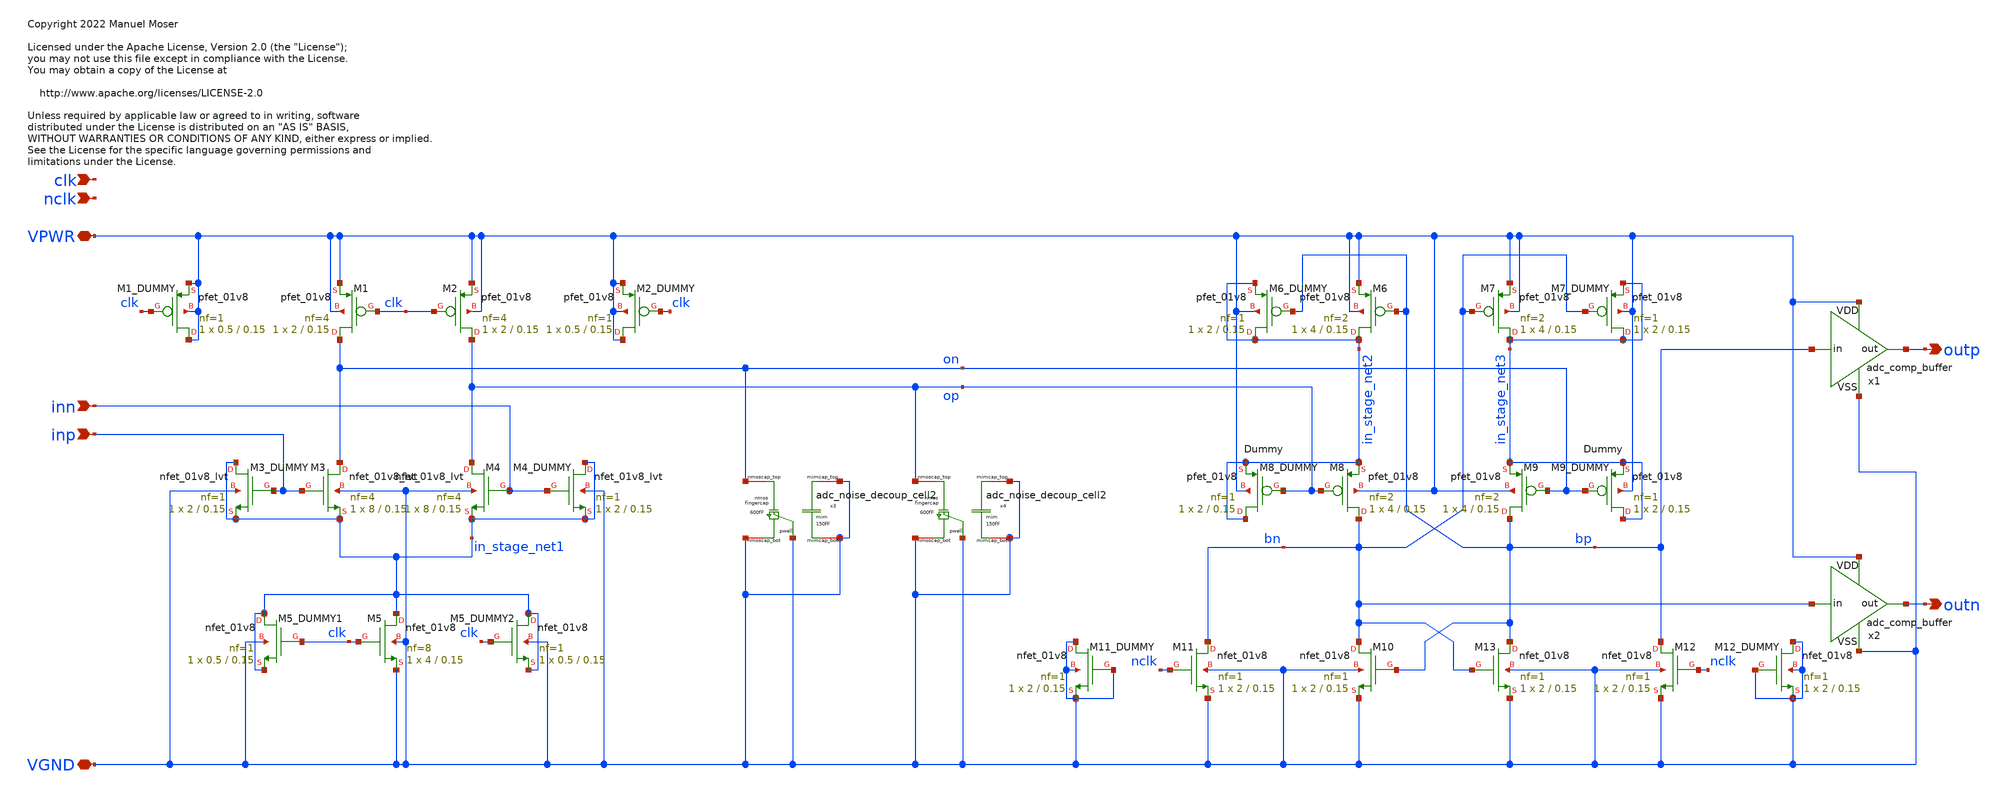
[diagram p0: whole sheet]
** sch_path: xschem/adc_comp_circuit.sch
* Copyright 2022 Manuel Moser
* Licensed under the Apache License, Version 2.0 (the "License");
**.subckt adc_comp_circuit VPWR VGND clk nclk inp inn outp outn
*.iopin VPWR
*.iopin VGND
*.ipin clk
*.ipin nclk
*.ipin inp
*.ipin inn
*.opin outp
*.opin outn
XM3 on inp in_stage_net1 VGND sky130_fd_pr__nfet_01v8_lvt L=0.15 W=8 nf=4 ad='int((nf+1)/2) * W/nf * 0.29'
+ as='int((nf+2)/2) * W/nf * 0.29' pd='2*int((nf+1)/2) * (W/nf + 0.29)' ps='2*int((nf+2)/2) * (W/nf + 0.29)'
+ nrd='0.29 / W' nrs='0.29 / W' sa=0 sb=0 sd=0 mult=1 m=1
XM4 op inn in_stage_net1 VGND sky130_fd_pr__nfet_01v8_lvt L=0.15 W=8 nf=4 ad='int((nf+1)/2) * W/nf * 0.29'
+ as='int((nf+2)/2) * W/nf * 0.29' pd='2*int((nf+1)/2) * (W/nf + 0.29)' ps='2*int((nf+2)/2) * (W/nf + 0.29)'
+ nrd='0.29 / W' nrs='0.29 / W' sa=0 sb=0 sd=0 mult=1 m=1
XM5 in_stage_net1 clk VGND VGND sky130_fd_pr__nfet_01v8 L=0.15 W=4 nf=8 ad='int((nf+1)/2) * W/nf * 0.29'
+ as='int((nf+2)/2) * W/nf * 0.29' pd='2*int((nf+1)/2) * (W/nf + 0.29)' ps='2*int((nf+2)/2) * (W/nf + 0.29)'
+ nrd='0.29 / W' nrs='0.29 / W' sa=0 sb=0 sd=0 mult=1 m=1
XM6 in_stage_net2 bp VPWR VPWR sky130_fd_pr__pfet_01v8 L=0.15 W=4 nf=2 ad='int((nf+1)/2) * W/nf * 0.29'
+ as='int((nf+2)/2) * W/nf * 0.29' pd='2*int((nf+1)/2) * (W/nf + 0.29)' ps='2*int((nf+2)/2) * (W/nf + 0.29)'
+ nrd='0.29 / W' nrs='0.29 / W' sa=0 sb=0 sd=0 mult=1 m=1
XM7 in_stage_net3 bn VPWR VPWR sky130_fd_pr__pfet_01v8 L=0.15 W=4 nf=2 ad='int((nf+1)/2) * W/nf * 0.29'
+ as='int((nf+2)/2) * W/nf * 0.29' pd='2*int((nf+1)/2) * (W/nf + 0.29)' ps='2*int((nf+2)/2) * (W/nf + 0.29)'
+ nrd='0.29 / W' nrs='0.29 / W' sa=0 sb=0 sd=0 mult=1 m=1
XM8 bn op in_stage_net2 VPWR sky130_fd_pr__pfet_01v8 L=0.15 W=4 nf=2 ad='int((nf+1)/2) * W/nf * 0.29'
+ as='int((nf+2)/2) * W/nf * 0.29' pd='2*int((nf+1)/2) * (W/nf + 0.29)' ps='2*int((nf+2)/2) * (W/nf + 0.29)'
+ nrd='0.29 / W' nrs='0.29 / W' sa=0 sb=0 sd=0 mult=1 m=1
XM9 bp on in_stage_net3 VPWR sky130_fd_pr__pfet_01v8 L=0.15 W=4 nf=2 ad='int((nf+1)/2) * W/nf * 0.29'
+ as='int((nf+2)/2) * W/nf * 0.29' pd='2*int((nf+1)/2) * (W/nf + 0.29)' ps='2*int((nf+2)/2) * (W/nf + 0.29)'
+ nrd='0.29 / W' nrs='0.29 / W' sa=0 sb=0 sd=0 mult=1 m=1
XM10 bn bp VGND VGND sky130_fd_pr__nfet_01v8 L=0.15 W=2 nf=1 ad='int((nf+1)/2) * W/nf * 0.29' as='int((nf+2)/2) * W/nf * 0.29'
+ pd='2*int((nf+1)/2) * (W/nf + 0.29)' ps='2*int((nf+2)/2) * (W/nf + 0.29)' nrd='0.29 / W' nrs='0.29 / W'
+ sa=0 sb=0 sd=0 mult=1 m=1
XM11 bn nclk VGND VGND sky130_fd_pr__nfet_01v8 L=0.15 W=2 nf=1 ad='int((nf+1)/2) * W/nf * 0.29' as='int((nf+2)/2) * W/nf * 0.29'
+ pd='2*int((nf+1)/2) * (W/nf + 0.29)' ps='2*int((nf+2)/2) * (W/nf + 0.29)' nrd='0.29 / W' nrs='0.29 / W'
+ sa=0 sb=0 sd=0 mult=1 m=1
XM12 bp nclk VGND VGND sky130_fd_pr__nfet_01v8 L=0.15 W=2 nf=1 ad='int((nf+1)/2) * W/nf * 0.29' as='int((nf+2)/2) * W/nf * 0.29'
+ pd='2*int((nf+1)/2) * (W/nf + 0.29)' ps='2*int((nf+2)/2) * (W/nf + 0.29)' nrd='0.29 / W' nrs='0.29 / W'
+ sa=0 sb=0 sd=0 mult=1 m=1
XM13 bp bn VGND VGND sky130_fd_pr__nfet_01v8 L=0.15 W=2 nf=1 ad='int((nf+1)/2) * W/nf * 0.29' as='int((nf+2)/2) * W/nf * 0.29'
+ pd='2*int((nf+1)/2) * (W/nf + 0.29)' ps='2*int((nf+2)/2) * (W/nf + 0.29)' nrd='0.29 / W' nrs='0.29 / W'
+ sa=0 sb=0 sd=0 mult=1 m=1
XM2 op clk VPWR VPWR sky130_fd_pr__pfet_01v8 L=0.15 W=2 nf=4 ad='int((nf+1)/2) * W/nf * 0.29' as='int((nf+2)/2) * W/nf * 0.29'
+ pd='2*int((nf+1)/2) * (W/nf + 0.29)' ps='2*int((nf+2)/2) * (W/nf + 0.29)' nrd='0.29 / W' nrs='0.29 / W'
+ sa=0 sb=0 sd=0 mult=1 m=1
XM1 on clk VPWR VPWR sky130_fd_pr__pfet_01v8 L=0.15 W=2 nf=4 ad='int((nf+1)/2) * W/nf * 0.29' as='int((nf+2)/2) * W/nf * 0.29'
+ pd='2*int((nf+1)/2) * (W/nf + 0.29)' ps='2*int((nf+2)/2) * (W/nf + 0.29)' nrd='0.29 / W' nrs='0.29 / W'
+ sa=0 sb=0 sd=0 mult=1 m=1
x1 VPWR VGND bp outp adc_comp_buffer
x2 VPWR VGND bn outn adc_comp_buffer
x3 VGND VGND on VGND VGND adc_noise_decoup_cell2
x4 VGND VGND op VGND VGND adc_noise_decoup_cell2
XM4_DUMMY in_stage_net1 inn in_stage_net1 VGND sky130_fd_pr__nfet_01v8_lvt L=0.15 W=2 nf=1 ad='int((nf+1)/2) * W/nf * 0.29'
+ as='int((nf+2)/2) * W/nf * 0.29' pd='2*int((nf+1)/2) * (W/nf + 0.29)' ps='2*int((nf+2)/2) * (W/nf + 0.29)'
+ nrd='0.29 / W' nrs='0.29 / W' sa=0 sb=0 sd=0 mult=1 m=1
XM3_DUMMY in_stage_net1 inp in_stage_net1 VGND sky130_fd_pr__nfet_01v8_lvt L=0.15 W=2 nf=1 ad='int((nf+1)/2) * W/nf * 0.29'
+ as='int((nf+2)/2) * W/nf * 0.29' pd='2*int((nf+1)/2) * (W/nf + 0.29)' ps='2*int((nf+2)/2) * (W/nf + 0.29)'
+ nrd='0.29 / W' nrs='0.29 / W' sa=0 sb=0 sd=0 mult=1 m=1
XM5_DUMMY2 in_stage_net1 clk in_stage_net1 VGND sky130_fd_pr__nfet_01v8 L=0.15 W=0.5 nf=1 ad='int((nf+1)/2) * W/nf * 0.29'
+ as='int((nf+2)/2) * W/nf * 0.29' pd='2*int((nf+1)/2) * (W/nf + 0.29)' ps='2*int((nf+2)/2) * (W/nf + 0.29)'
+ nrd='0.29 / W' nrs='0.29 / W' sa=0 sb=0 sd=0 mult=1 m=1
XM5_DUMMY1 in_stage_net1 clk in_stage_net1 VGND sky130_fd_pr__nfet_01v8 L=0.15 W=0.5 nf=1 ad='int((nf+1)/2) * W/nf * 0.29'
+ as='int((nf+2)/2) * W/nf * 0.29' pd='2*int((nf+1)/2) * (W/nf + 0.29)' ps='2*int((nf+2)/2) * (W/nf + 0.29)'
+ nrd='0.29 / W' nrs='0.29 / W' sa=0 sb=0 sd=0 mult=1 m=1
XM2_DUMMY VPWR clk VPWR VPWR sky130_fd_pr__pfet_01v8 L=0.15 W=0.5 nf=1 ad='int((nf+1)/2) * W/nf * 0.29'
+ as='int((nf+2)/2) * W/nf * 0.29' pd='2*int((nf+1)/2) * (W/nf + 0.29)' ps='2*int((nf+2)/2) * (W/nf + 0.29)'
+ nrd='0.29 / W' nrs='0.29 / W' sa=0 sb=0 sd=0 mult=1 m=1
XM1_DUMMY VPWR clk VPWR VPWR sky130_fd_pr__pfet_01v8 L=0.15 W=0.5 nf=1 ad='int((nf+1)/2) * W/nf * 0.29'
+ as='int((nf+2)/2) * W/nf * 0.29' pd='2*int((nf+1)/2) * (W/nf + 0.29)' ps='2*int((nf+2)/2) * (W/nf + 0.29)'
+ nrd='0.29 / W' nrs='0.29 / W' sa=0 sb=0 sd=0 mult=1 m=1
XM8_DUMMY in_stage_net2 op in_stage_net2 VPWR sky130_fd_pr__pfet_01v8 L=0.15 W=2 nf=1 ad='int((nf+1)/2) * W/nf * 0.29'
+ as='int((nf+2)/2) * W/nf * 0.29' pd='2*int((nf+1)/2) * (W/nf + 0.29)' ps='2*int((nf+2)/2) * (W/nf + 0.29)'
+ nrd='0.29 / W' nrs='0.29 / W' sa=0 sb=0 sd=0 mult=1 m=1
XM9_DUMMY in_stage_net3 on in_stage_net3 VPWR sky130_fd_pr__pfet_01v8 L=0.15 W=2 nf=1 ad='int((nf+1)/2) * W/nf * 0.29'
+ as='int((nf+2)/2) * W/nf * 0.29' pd='2*int((nf+1)/2) * (W/nf + 0.29)' ps='2*int((nf+2)/2) * (W/nf + 0.29)'
+ nrd='0.29 / W' nrs='0.29 / W' sa=0 sb=0 sd=0 mult=1 m=1
XM6_DUMMY in_stage_net2 bp in_stage_net2 VPWR sky130_fd_pr__pfet_01v8 L=0.15 W=2 nf=1 ad='int((nf+1)/2) * W/nf * 0.29'
+ as='int((nf+2)/2) * W/nf * 0.29' pd='2*int((nf+1)/2) * (W/nf + 0.29)' ps='2*int((nf+2)/2) * (W/nf + 0.29)'
+ nrd='0.29 / W' nrs='0.29 / W' sa=0 sb=0 sd=0 mult=1 m=1
XM7_DUMMY in_stage_net3 bn in_stage_net3 VPWR sky130_fd_pr__pfet_01v8 L=0.15 W=2 nf=1 ad='int((nf+1)/2) * W/nf * 0.29'
+ as='int((nf+2)/2) * W/nf * 0.29' pd='2*int((nf+1)/2) * (W/nf + 0.29)' ps='2*int((nf+2)/2) * (W/nf + 0.29)'
+ nrd='0.29 / W' nrs='0.29 / W' sa=0 sb=0 sd=0 mult=1 m=1
XM12_DUMMY VGND VGND VGND VGND sky130_fd_pr__nfet_01v8 L=0.15 W=2 nf=1 ad='int((nf+1)/2) * W/nf * 0.29'
+ as='int((nf+2)/2) * W/nf * 0.29' pd='2*int((nf+1)/2) * (W/nf + 0.29)' ps='2*int((nf+2)/2) * (W/nf + 0.29)'
+ nrd='0.29 / W' nrs='0.29 / W' sa=0 sb=0 sd=0 mult=1 m=1
XM11_DUMMY VGND VGND VGND VGND sky130_fd_pr__nfet_01v8 L=0.15 W=2 nf=1 ad='int((nf+1)/2) * W/nf * 0.29'
+ as='int((nf+2)/2) * W/nf * 0.29' pd='2*int((nf+1)/2) * (W/nf + 0.29)' ps='2*int((nf+2)/2) * (W/nf + 0.29)'
+ nrd='0.29 / W' nrs='0.29 / W' sa=0 sb=0 sd=0 mult=1 m=1
**.ends

* expanding   symbol:  adc_comp_buffer.sym # of pins=4
** sym_path: xschem/adc_comp_buffer.sym
** sch_path: xschem/adc_comp_buffer.sch
.subckt adc_comp_buffer VDD VSS in out
*.iopin VDD
*.iopin VSS
*.ipin in
*.opin out
XM5 net1 in VSS VSS sky130_fd_pr__nfet_01v8 L=0.15 W=0.5 nf=1 ad='int((nf+1)/2) * W/nf * 0.29' as='int((nf+2)/2) * W/nf * 0.29'
+ pd='2*int((nf+1)/2) * (W/nf + 0.29)' ps='2*int((nf+2)/2) * (W/nf + 0.29)' nrd='0.29 / W' nrs='0.29 / W'
+ sa=0 sb=0 sd=0 mult=1 m=1
XM1 net1 in VDD VDD sky130_fd_pr__pfet_01v8 L=0.15 W=1 nf=1 ad='int((nf+1)/2) * W/nf * 0.29' as='int((nf+2)/2) * W/nf * 0.29'
+ pd='2*int((nf+1)/2) * (W/nf + 0.29)' ps='2*int((nf+2)/2) * (W/nf + 0.29)' nrd='0.29 / W' nrs='0.29 / W'
+ sa=0 sb=0 sd=0 mult=1 m=1
XM2 out net1 VDD VDD sky130_fd_pr__pfet_01v8 L=0.15 W=2 nf=2 ad='int((nf+1)/2) * W/nf * 0.29' as='int((nf+2)/2) * W/nf * 0.29'
+ pd='2*int((nf+1)/2) * (W/nf + 0.29)' ps='2*int((nf+2)/2) * (W/nf + 0.29)' nrd='0.29 / W' nrs='0.29 / W'
+ sa=0 sb=0 sd=0 mult=1 m=1
XM6 out net1 VSS VSS sky130_fd_pr__nfet_01v8 L=0.15 W=1 nf=2 ad='int((nf+1)/2) * W/nf * 0.29' as='int((nf+2)/2) * W/nf * 0.29'
+ pd='2*int((nf+1)/2) * (W/nf + 0.29)' ps='2*int((nf+2)/2) * (W/nf + 0.29)' nrd='0.29 / W' nrs='0.29 / W'
+ sa=0 sb=0 sd=0 mult=1 m=1
.ends


* expanding   symbol:  adc_noise_decoup_cell2.sym # of pins=5
** sym_path: xschem/adc_noise_decoup_cell2.sym
** sch_path: xschem/adc_noise_decoup_cell2.sch
.subckt adc_noise_decoup_cell2 mimcap_top mimcap_bot nmoscap_top nmoscap_bot pwell
*.iopin nmoscap_top
*.iopin mimcap_top
*.iopin mimcap_bot
*.iopin nmoscap_bot
*.iopin pwell
XC1 mimcap_top mimcap_bot sky130_fd_pr__cap_mim_m3_1 W=18.9 L=5.1 MF=1 m=1
XC2 nmoscap_top nmoscap_bot pwell sky130_fd_pr__cap_var_lvt W=18.4 L=3.9 VM=1 m=1
.ends

.end
